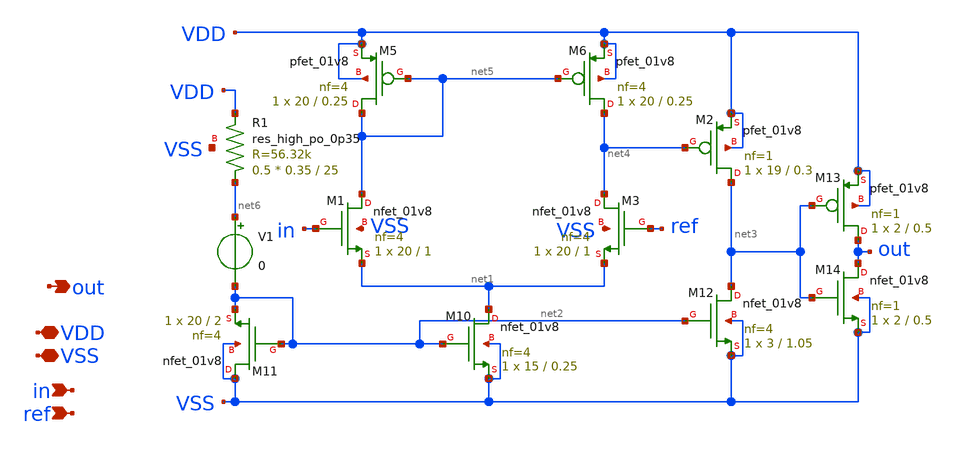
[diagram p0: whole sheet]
** sch_path: xschem/src/comparator2/comparator2.sch
**.subckt comparator2 VDD in out VSS ref
*.iopin VDD
*.ipin in
*.opin out
*.iopin VSS
*.ipin ref
XM5 net5 net5 VDD VDD sky130_fd_pr__pfet_01v8 L=0.25 W=20 nf=4 ad='int((nf+1)/2) * W/nf * 0.29' as='int((nf+2)/2) * W/nf * 0.29'
+ pd='2*int((nf+1)/2) * (W/nf + 0.29)' ps='2*int((nf+2)/2) * (W/nf + 0.29)' nrd='0.29 / W' nrs='0.29 / W'
+ sa=0 sb=0 sd=0 mult=1 m=1
XM6 net4 net5 VDD VDD sky130_fd_pr__pfet_01v8 L=0.25 W=20 nf=4 ad='int((nf+1)/2) * W/nf * 0.29' as='int((nf+2)/2) * W/nf * 0.29'
+ pd='2*int((nf+1)/2) * (W/nf + 0.29)' ps='2*int((nf+2)/2) * (W/nf + 0.29)' nrd='0.29 / W' nrs='0.29 / W'
+ sa=0 sb=0 sd=0 mult=1 m=1
XM10 net1 net2 VSS VSS sky130_fd_pr__nfet_01v8 L=0.25 W=15 nf=4 ad='int((nf+1)/2) * W/nf * 0.29' as='int((nf+2)/2) * W/nf * 0.29'
+ pd='2*int((nf+1)/2) * (W/nf + 0.29)' ps='2*int((nf+2)/2) * (W/nf + 0.29)' nrd='0.29 / W' nrs='0.29 / W'
+ sa=0 sb=0 sd=0 mult=1 m=1
XM11 VSS net2 net2 VSS sky130_fd_pr__nfet_01v8 L=2 W=20 nf=4 ad='int((nf+1)/2) * W/nf * 0.29' as='int((nf+2)/2) * W/nf * 0.29'
+ pd='2*int((nf+1)/2) * (W/nf + 0.29)' ps='2*int((nf+2)/2) * (W/nf + 0.29)' nrd='0.29 / W' nrs='0.29 / W'
+ sa=0 sb=0 sd=0 mult=1 m=1
XM12 net3 net2 VSS VSS sky130_fd_pr__nfet_01v8 L=1.05 W=3 nf=4 ad='int((nf+1)/2) * W/nf * 0.29' as='int((nf+2)/2) * W/nf * 0.29'
+ pd='2*int((nf+1)/2) * (W/nf + 0.29)' ps='2*int((nf+2)/2) * (W/nf + 0.29)' nrd='0.29 / W' nrs='0.29 / W'
+ sa=0 sb=0 sd=0 mult=1 m=1
XM13 out net3 VDD VDD sky130_fd_pr__pfet_01v8 L=0.5 W=2 nf=1 ad='int((nf+1)/2) * W/nf * 0.29' as='int((nf+2)/2) * W/nf * 0.29'
+ pd='2*int((nf+1)/2) * (W/nf + 0.29)' ps='2*int((nf+2)/2) * (W/nf + 0.29)' nrd='0.29 / W' nrs='0.29 / W'
+ sa=0 sb=0 sd=0 mult=1 m=1
XM14 out net3 VSS VSS sky130_fd_pr__nfet_01v8 L=0.5 W=2 nf=1 ad='int((nf+1)/2) * W/nf * 0.29' as='int((nf+2)/2) * W/nf * 0.29'
+ pd='2*int((nf+1)/2) * (W/nf + 0.29)' ps='2*int((nf+2)/2) * (W/nf + 0.29)' nrd='0.29 / W' nrs='0.29 / W'
+ sa=0 sb=0 sd=0 mult=1 m=1
XM2 net3 net4 VDD VDD sky130_fd_pr__pfet_01v8 L=0.3 W=19 nf=1 ad='int((nf+1)/2) * W/nf * 0.29' as='int((nf+2)/2) * W/nf * 0.29'
+ pd='2*int((nf+1)/2) * (W/nf + 0.29)' ps='2*int((nf+2)/2) * (W/nf + 0.29)' nrd='0.29 / W' nrs='0.29 / W'
+ sa=0 sb=0 sd=0 mult=1 m=1
XM1 net5 in net1 VSS sky130_fd_pr__nfet_01v8 L=1 W=20 nf=4 ad='int((nf+1)/2) * W/nf * 0.29' as='int((nf+2)/2) * W/nf * 0.29'
+ pd='2*int((nf+1)/2) * (W/nf + 0.29)' ps='2*int((nf+2)/2) * (W/nf + 0.29)' nrd='0.29 / W' nrs='0.29 / W'
+ sa=0 sb=0 sd=0 mult=1 m=1
XM3 net4 ref net1 VSS sky130_fd_pr__nfet_01v8 L=1 W=20 nf=4 ad='int((nf+1)/2) * W/nf * 0.29' as='int((nf+2)/2) * W/nf * 0.29'
+ pd='2*int((nf+1)/2) * (W/nf + 0.29)' ps='2*int((nf+2)/2) * (W/nf + 0.29)' nrd='0.29 / W' nrs='0.29 / W'
+ sa=0 sb=0 sd=0 mult=1 m=1
XR1 net6 VDD VSS sky130_fd_pr__res_high_po_0p35 L=25 mult=0.5 m=0.5
V1 net6 net2 0
**.ends
.end
